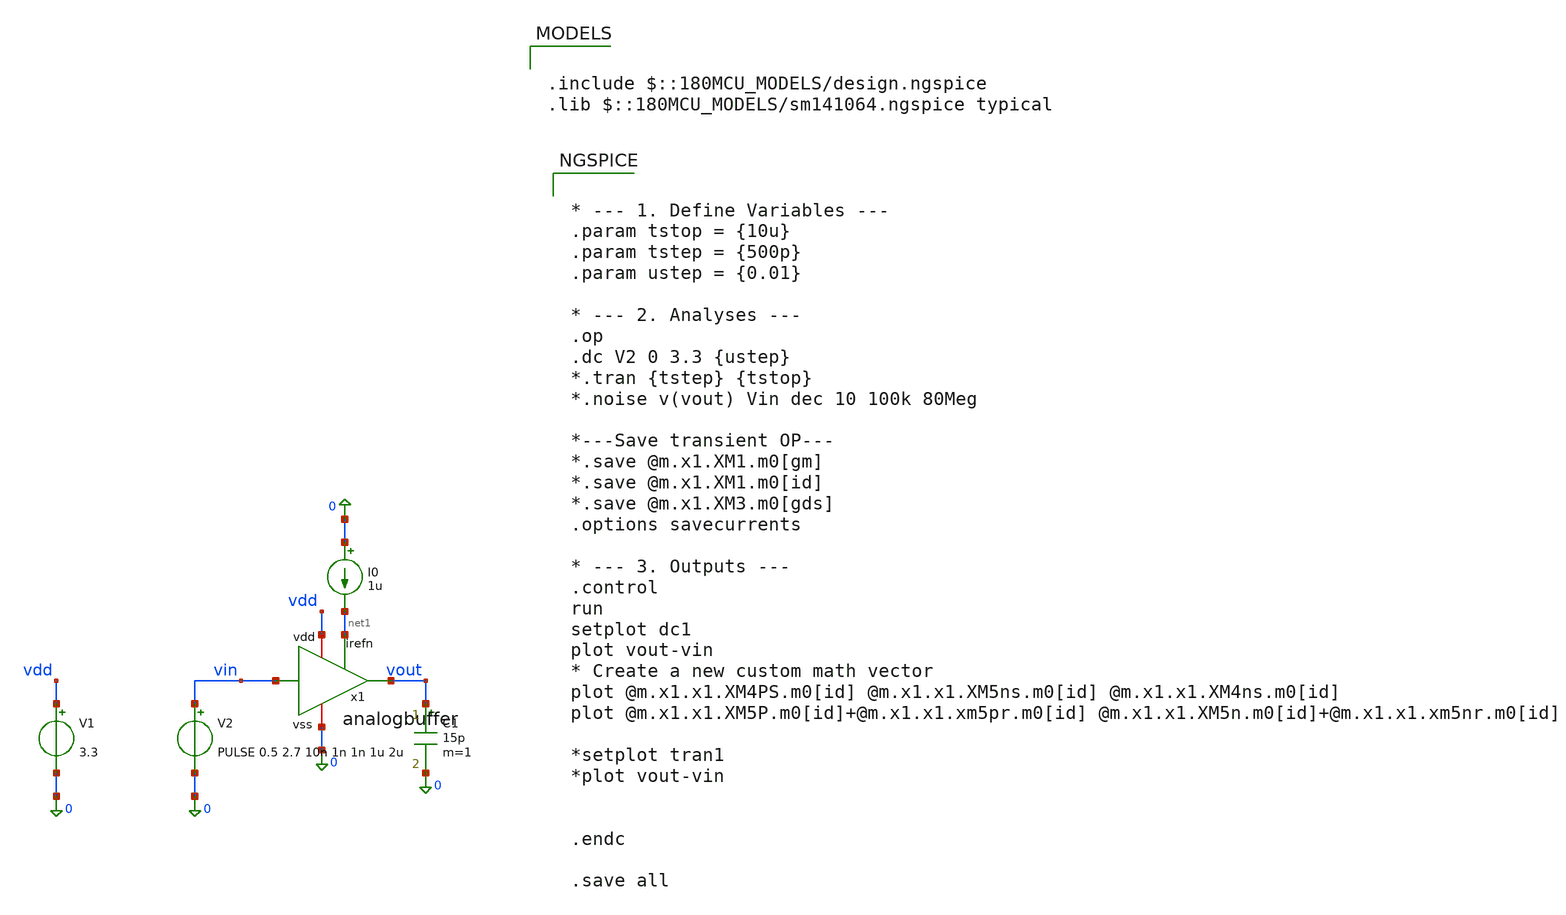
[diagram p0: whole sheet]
** sch_path: Tobias/2026 07 16 Results/analogbuffer/analogbuffer-tb.sch
**.subckt analogbuffer-tb
x1 vdd net1 vin vout 0 analogbuffer
I0 0 net1 1u
V1 vdd 0 3.3
V2 vin 0 PULSE 0.5 2.7 10n 1n 1n 1u 2u
C1 vout 0 15p m=1
**** begin user architecture code


* --- 1. Define Variables ---
.param tstop = {10u}
.param tstep = {500p}
.param ustep = {0.01}

* --- 2. Analyses ---
.op
.dc V2 0 3.3 {ustep}
*.tran {tstep} {tstop}
*.noise v(vout) Vin dec 10 100k 80Meg

*---Save transient OP---
*.save @m.x1.XM1.m0[gm]
*.save @m.x1.XM1.m0[id]
*.save @m.x1.XM3.m0[gds]
.options savecurrents

* --- 3. Outputs ---
.control
run
setplot dc1
plot vout-vin
* Create a new custom math vector
plot @m.x1.x1.XM4PS.m0[id] @m.x1.x1.XM5ns.m0[id] @m.x1.x1.XM4ns.m0[id]
plot @m.x1.x1.XM5P.m0[id]+@m.x1.x1.xm5pr.m0[id] @m.x1.x1.XM5n.m0[id]+@m.x1.x1.xm5nr.m0[id]

*setplot tran1
*plot vout-vin


.endc

.save all



.include $::180MCU_MODELS/design.ngspice
.lib $::180MCU_MODELS/sm141064.ngspice typical

**** end user architecture code
**.ends
.end
